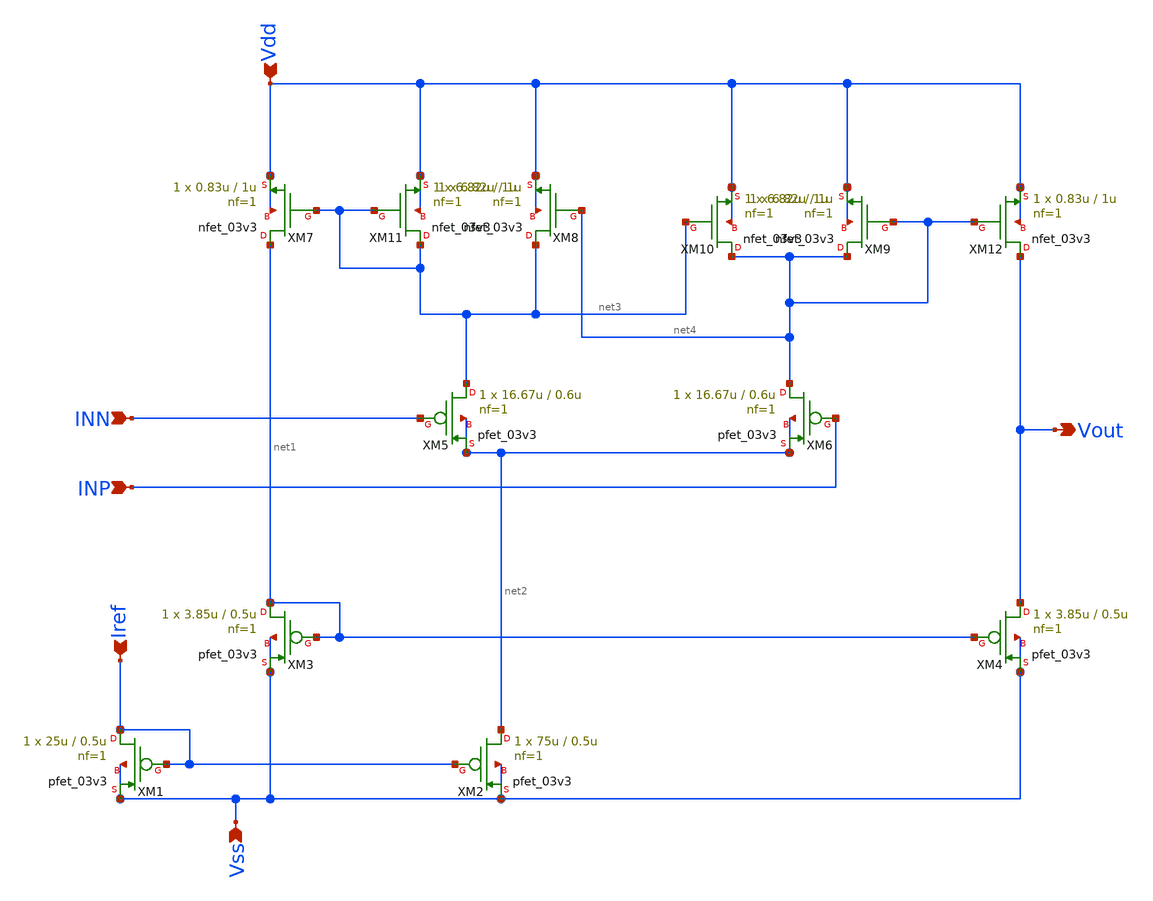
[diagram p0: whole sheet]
** sch_path: designs/libs/core_analog/Comparator/Pmos_Comparator.sch
**.subckt Pmos_Comparator Vss Vdd Iref INN INP Vout
*.ipin Vss
*.ipin Vdd
*.ipin Iref
*.ipin INN
*.ipin INP
*.opin Vout
XM1 Iref Iref Vss Vss pfet_03v3 L=0.5u W=25u nf=1 ad='int((nf+1)/2) * W/nf * 0.18u' as='int((nf+2)/2) * W/nf * 0.18u'
+ pd='2*int((nf+1)/2) * (W/nf + 0.18u)' ps='2*int((nf+2)/2) * (W/nf + 0.18u)' nrd='0.18u / W' nrs='0.18u / W'
+ sa=0 sb=0 sd=0 m=1
XM2 net2 Iref Vss Vss pfet_03v3 L=0.5u W=75u nf=1 ad='int((nf+1)/2) * W/nf * 0.18u' as='int((nf+2)/2) * W/nf * 0.18u'
+ pd='2*int((nf+1)/2) * (W/nf + 0.18u)' ps='2*int((nf+2)/2) * (W/nf + 0.18u)' nrd='0.18u / W' nrs='0.18u / W'
+ sa=0 sb=0 sd=0 m=1
XM3 net1 net1 Vss Vss pfet_03v3 L=0.5u W=3.85u nf=1 ad='int((nf+1)/2) * W/nf * 0.18u' as='int((nf+2)/2) * W/nf * 0.18u'
+ pd='2*int((nf+1)/2) * (W/nf + 0.18u)' ps='2*int((nf+2)/2) * (W/nf + 0.18u)' nrd='0.18u / W' nrs='0.18u / W'
+ sa=0 sb=0 sd=0 m=1
XM4 Vout net1 Vss Vss pfet_03v3 L=0.5u W=3.85u nf=1 ad='int((nf+1)/2) * W/nf * 0.18u' as='int((nf+2)/2) * W/nf * 0.18u'
+ pd='2*int((nf+1)/2) * (W/nf + 0.18u)' ps='2*int((nf+2)/2) * (W/nf + 0.18u)' nrd='0.18u / W' nrs='0.18u / W'
+ sa=0 sb=0 sd=0 m=1
XM5 net3 INN net2 net2 pfet_03v3 L=0.6u W=16.67u nf=1 ad='int((nf+1)/2) * W/nf * 0.18u' as='int((nf+2)/2) * W/nf * 0.18u'
+ pd='2*int((nf+1)/2) * (W/nf + 0.18u)' ps='2*int((nf+2)/2) * (W/nf + 0.18u)' nrd='0.18u / W' nrs='0.18u / W'
+ sa=0 sb=0 sd=0 m=1
XM6 net4 INP net2 net2 pfet_03v3 L=0.6u W=16.67u nf=1 ad='int((nf+1)/2) * W/nf * 0.18u' as='int((nf+2)/2) * W/nf * 0.18u'
+ pd='2*int((nf+1)/2) * (W/nf + 0.18u)' ps='2*int((nf+2)/2) * (W/nf + 0.18u)' nrd='0.18u / W' nrs='0.18u / W'
+ sa=0 sb=0 sd=0 m=1
XM7 net1 net3 Vdd Vdd nfet_03v3 L=1u W=0.83u nf=1 ad='int((nf+1)/2) * W/nf * 0.18u' as='int((nf+2)/2) * W/nf * 0.18u'
+ pd='2*int((nf+1)/2) * (W/nf + 0.18u)' ps='2*int((nf+2)/2) * (W/nf + 0.18u)' nrd='0.18u / W' nrs='0.18u / W'
+ sa=0 sb=0 sd=0 m=1
XM8 net3 net4 Vdd Vdd nfet_03v3 L=1u W=6.82u nf=1 ad='int((nf+1)/2) * W/nf * 0.18u' as='int((nf+2)/2) * W/nf * 0.18u'
+ pd='2*int((nf+1)/2) * (W/nf + 0.18u)' ps='2*int((nf+2)/2) * (W/nf + 0.18u)' nrd='0.18u / W' nrs='0.18u / W'
+ sa=0 sb=0 sd=0 m=1
XM9 net4 net4 Vdd Vdd nfet_03v3 L=1u W=6.82u nf=1 ad='int((nf+1)/2) * W/nf * 0.18u' as='int((nf+2)/2) * W/nf * 0.18u'
+ pd='2*int((nf+1)/2) * (W/nf + 0.18u)' ps='2*int((nf+2)/2) * (W/nf + 0.18u)' nrd='0.18u / W' nrs='0.18u / W'
+ sa=0 sb=0 sd=0 m=1
XM10 net4 net3 Vdd Vdd nfet_03v3 L=1u W=6.82u nf=1 ad='int((nf+1)/2) * W/nf * 0.18u' as='int((nf+2)/2) * W/nf * 0.18u'
+ pd='2*int((nf+1)/2) * (W/nf + 0.18u)' ps='2*int((nf+2)/2) * (W/nf + 0.18u)' nrd='0.18u / W' nrs='0.18u / W'
+ sa=0 sb=0 sd=0 m=1
XM11 net3 net3 Vdd Vdd nfet_03v3 L=1u W=6.82u nf=1 ad='int((nf+1)/2) * W/nf * 0.18u' as='int((nf+2)/2) * W/nf * 0.18u'
+ pd='2*int((nf+1)/2) * (W/nf + 0.18u)' ps='2*int((nf+2)/2) * (W/nf + 0.18u)' nrd='0.18u / W' nrs='0.18u / W'
+ sa=0 sb=0 sd=0 m=1
XM12 Vout net4 Vdd Vdd nfet_03v3 L=1u W=0.83u nf=1 ad='int((nf+1)/2) * W/nf * 0.18u' as='int((nf+2)/2) * W/nf * 0.18u'
+ pd='2*int((nf+1)/2) * (W/nf + 0.18u)' ps='2*int((nf+2)/2) * (W/nf + 0.18u)' nrd='0.18u / W' nrs='0.18u / W'
+ sa=0 sb=0 sd=0 m=1
**.ends
.end
